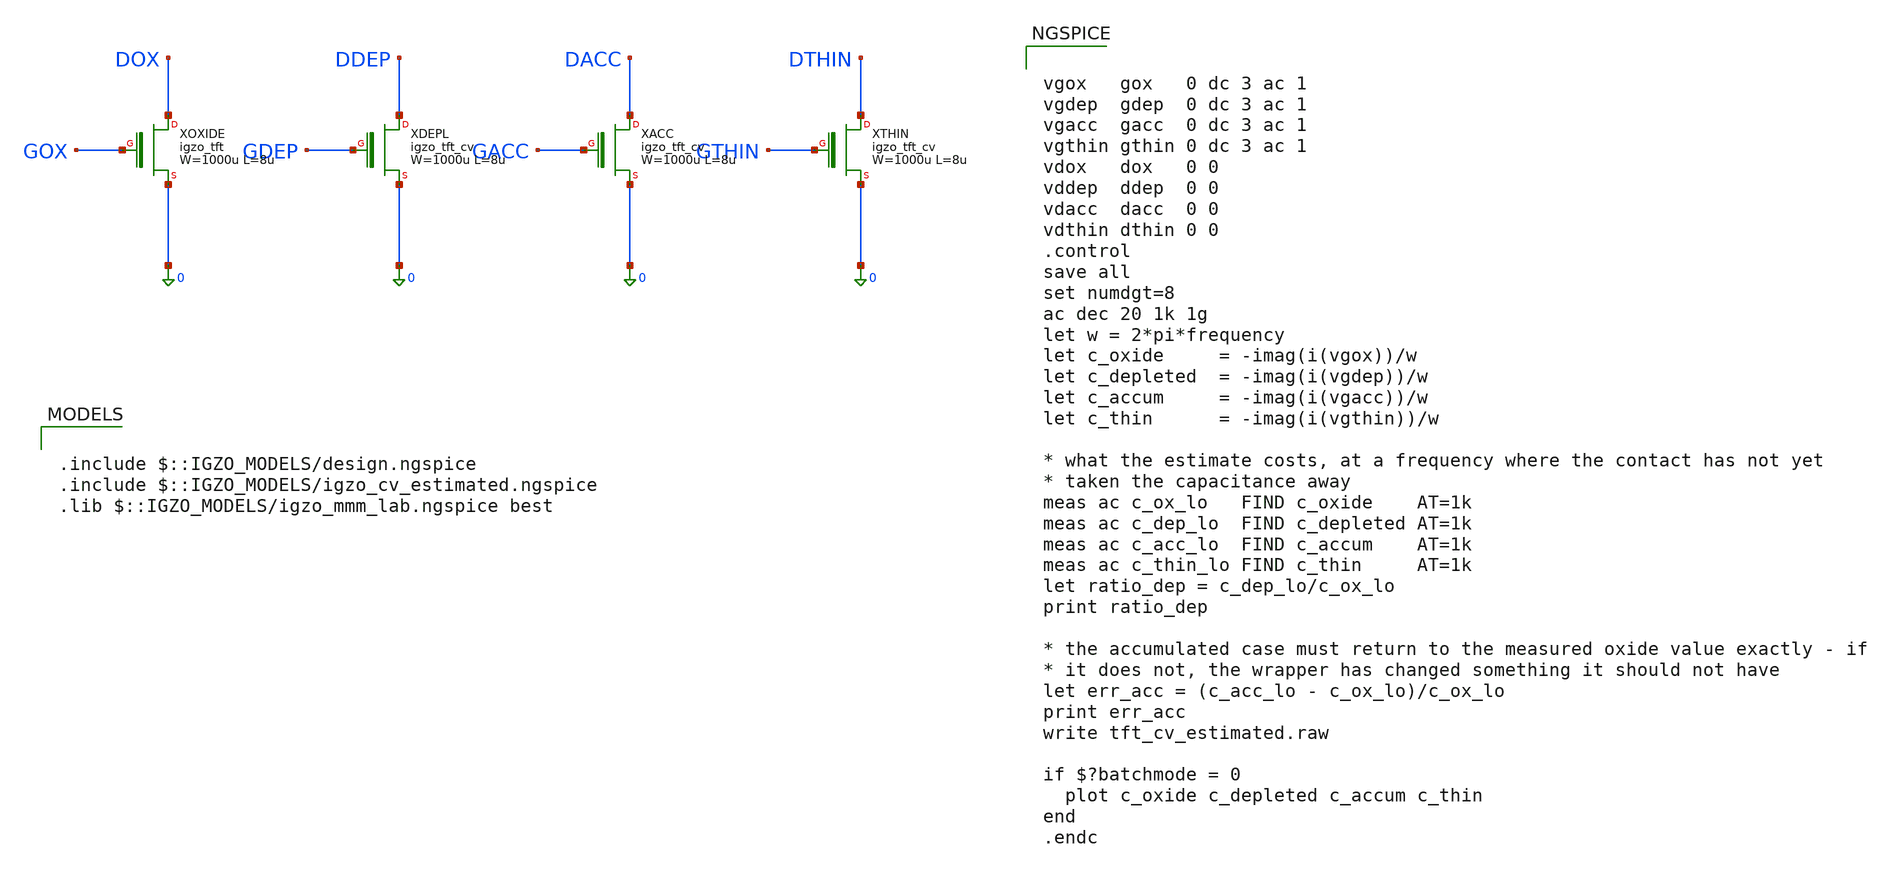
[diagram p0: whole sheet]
** sch_path: libs.tech/xschem/tests/tft_cv_estimated.sch
**.subckt tft_cv_estimated
XXOXIDE DOX GOX 0 igzo_tft W=1000u L=8u ov=5u nf=1 m=1
XXDEPL DDEP GDEP 0 igzo_tft_cv W=1000u L=8u ov=5u nf=1 m=1 B=0 b_scale=1 acc=0 t_igzo=30e-9 vdep=0
XXACC DACC GACC 0 igzo_tft_cv W=1000u L=8u ov=5u nf=1 m=1 B=0 b_scale=1 acc=1 t_igzo=30e-9 vdep=0
XXTHIN DTHIN GTHIN 0 igzo_tft_cv W=1000u L=8u ov=5u nf=1 m=1 B=0 b_scale=1 acc=0 t_igzo=15e-9 vdep=0
**** begin user architecture code

.include $::IGZO_MODELS/design.ngspice
.include $::IGZO_MODELS/igzo_cv_estimated.ngspice
.lib $::IGZO_MODELS/igzo_mmm_lab.ngspice best



vgox   gox   0 dc 3 ac 1
vgdep  gdep  0 dc 3 ac 1
vgacc  gacc  0 dc 3 ac 1
vgthin gthin 0 dc 3 ac 1
vdox   dox   0 0
vddep  ddep  0 0
vdacc  dacc  0 0
vdthin dthin 0 0
.control
save all
set numdgt=8
ac dec 20 1k 1g
let w = 2*pi*frequency
let c_oxide     = -imag(i(vgox))/w
let c_depleted  = -imag(i(vgdep))/w
let c_accum     = -imag(i(vgacc))/w
let c_thin      = -imag(i(vgthin))/w

* what the estimate costs, at a frequency where the contact has not yet
* taken the capacitance away
meas ac c_ox_lo   FIND c_oxide    AT=1k
meas ac c_dep_lo  FIND c_depleted AT=1k
meas ac c_acc_lo  FIND c_accum    AT=1k
meas ac c_thin_lo FIND c_thin     AT=1k
let ratio_dep = c_dep_lo/c_ox_lo
print ratio_dep

* the accumulated case must return to the measured oxide value exactly - if
* it does not, the wrapper has changed something it should not have
let err_acc = (c_acc_lo - c_ox_lo)/c_ox_lo
print err_acc
write tft_cv_estimated.raw

if $?batchmode = 0
  plot c_oxide c_depleted c_accum c_thin
end
.endc


**** end user architecture code
**.ends
.end
